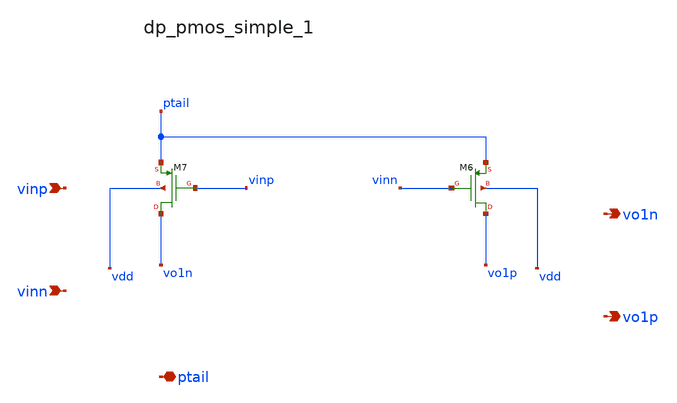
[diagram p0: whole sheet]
** sch_path: analog-db/raw/amp_031_srmc_core_cmfb/hier/blocks/dp_pmos_simple_1.sch
**.subckt dp_pmos_simple_1 vinp vinn ptail vo1n vo1p
*.ipin vinp
*.ipin vinn
*.iopin ptail
*.opin vo1n
*.opin vo1p
XM6 vo1p vinn ptail vdd sg13_lv_pmos w=x_dut_xm6_w l=x_dut_xm6_l ng=1 m=x_dut_xm6_m
XM7 vo1n vinp ptail vdd sg13_lv_pmos w=x_dut_xm7_w l=x_dut_xm7_l ng=1 m=x_dut_xm7_m
**.ends
.end
